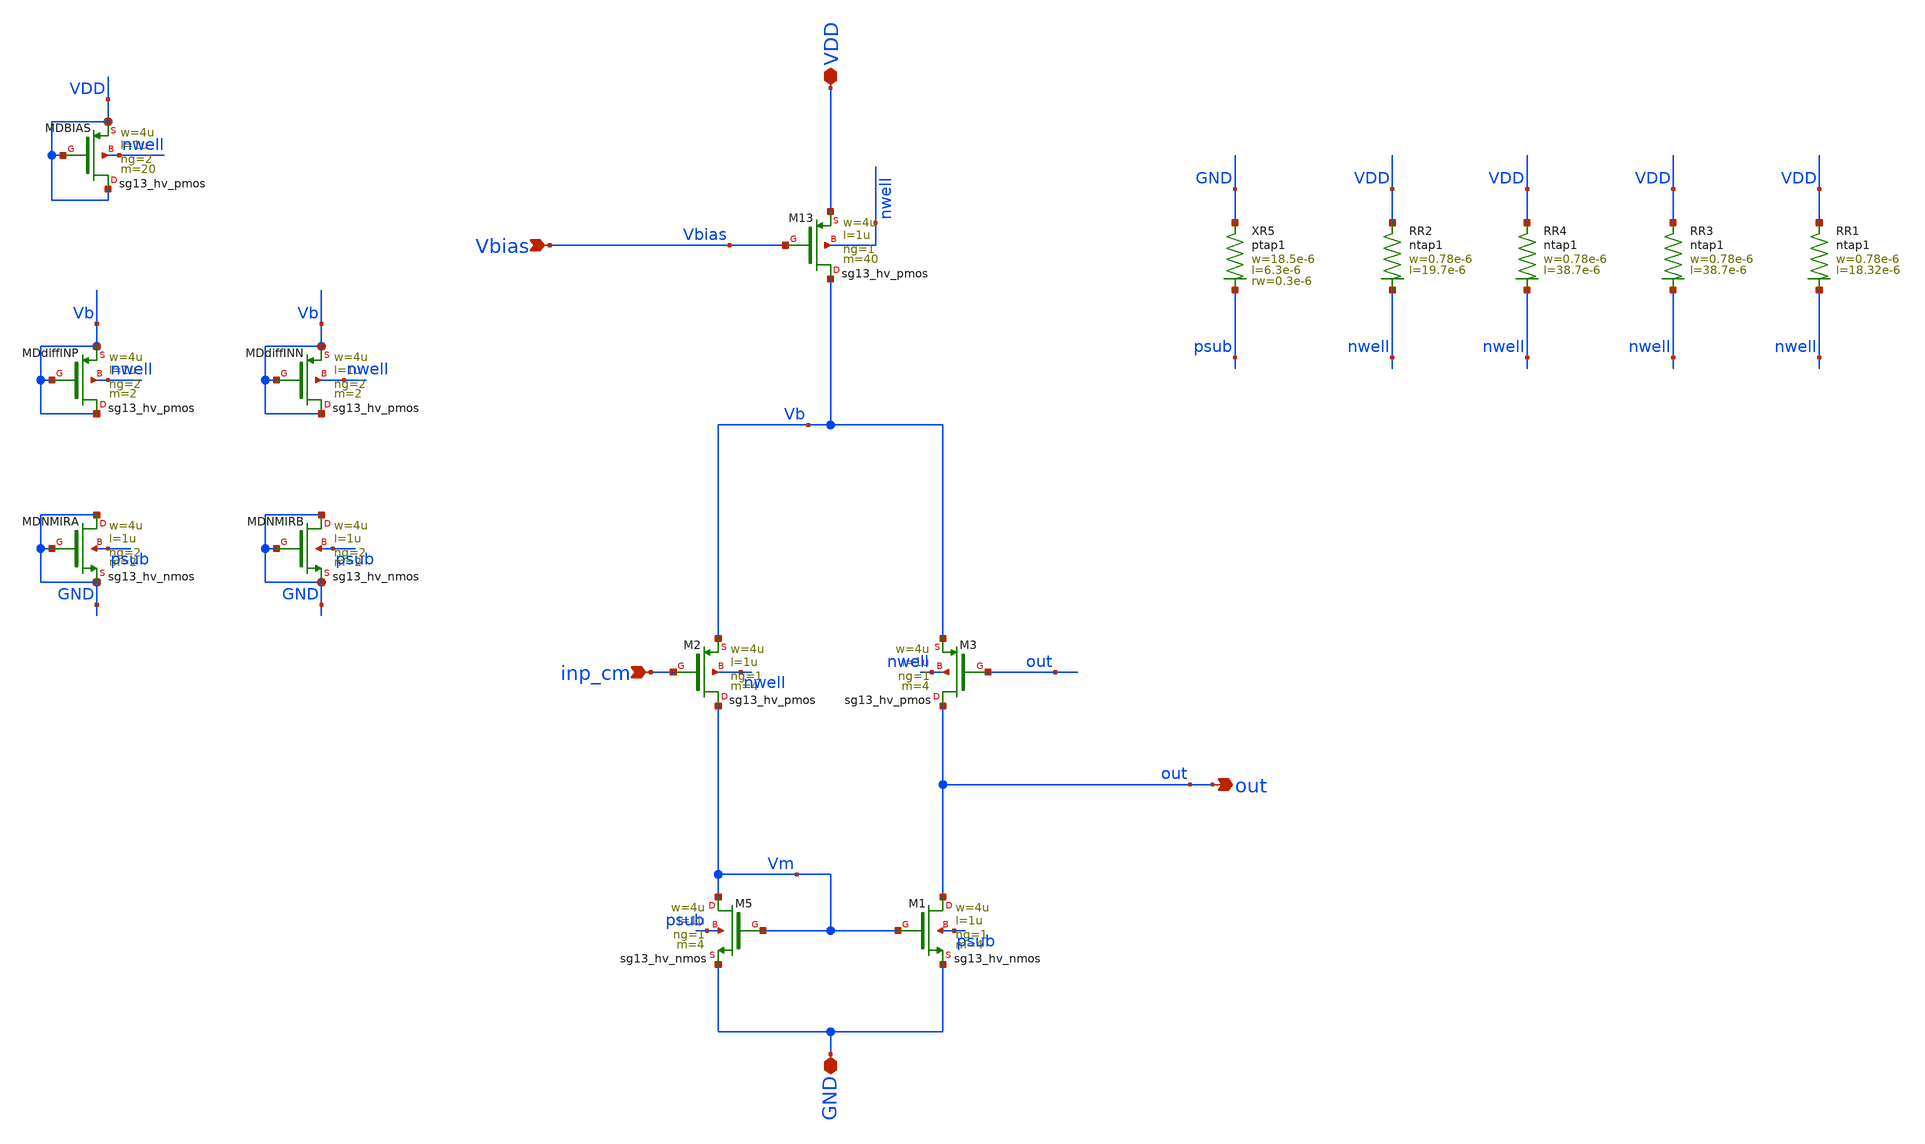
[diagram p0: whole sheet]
** sch_path: xschem/V2I/buffer_final.sch
**.subckt buffer_final inp_cm out VDD GND Vbias
*.ipin inp_cm
*.opin out
*.iopin VDD
*.iopin GND
*.ipin Vbias
XM2 Vm inp_cm Vb nwell sg13_hv_pmos w=4u l=1u ng=1 m=4 mm_ok=1
XM5 Vm Vm GND psub sg13_hv_nmos w=4u l=1u ng=1 m=4 mm_ok=1
XM13 Vb Vbias VDD nwell sg13_hv_pmos w=4u l=1u ng=1 m=40 mm_ok=1
XM3 out out Vb nwell sg13_hv_pmos w=4u l=1u ng=1 m=4 mm_ok=1
XM1 out Vm GND psub sg13_hv_nmos w=4u l=1u ng=1 m=4 mm_ok=1
XR2 VDD nwell ntap1 R=17.4 w=0.78e-6 l=19.7e-6
XMDBIAS VDD VDD VDD nwell sg13_hv_pmos w=4u l=1u ng=2 m=20 mm_ok=1
XMDdiffINP Vb Vb Vb nwell sg13_hv_pmos w=4u l=1u ng=2 m=2 mm_ok=1
XMDdiffINN Vb Vb Vb nwell sg13_hv_pmos w=4u l=1u ng=2 m=2 mm_ok=1
XMDNMIRA GND GND GND psub sg13_hv_nmos w=4u l=1u ng=2 m=2 mm_ok=1
XMDNMIRB GND GND GND psub sg13_hv_nmos w=4u l=1u ng=2 m=2 mm_ok=1
XR3 VDD nwell ntap1 R=8.979 w=0.78e-6 l=38.7e-6
XR4 VDD nwell ntap1 R=8.979 w=0.78e-6 l=38.7e-6
XR5 GND psub ptap1 R=4.709 w=18.5e-6 l=6.3e-6 rw=0.3e-6
XR1 VDD nwell ntap1 R=18.67 w=0.78e-6 l=18.32e-6
**.ends
.end
